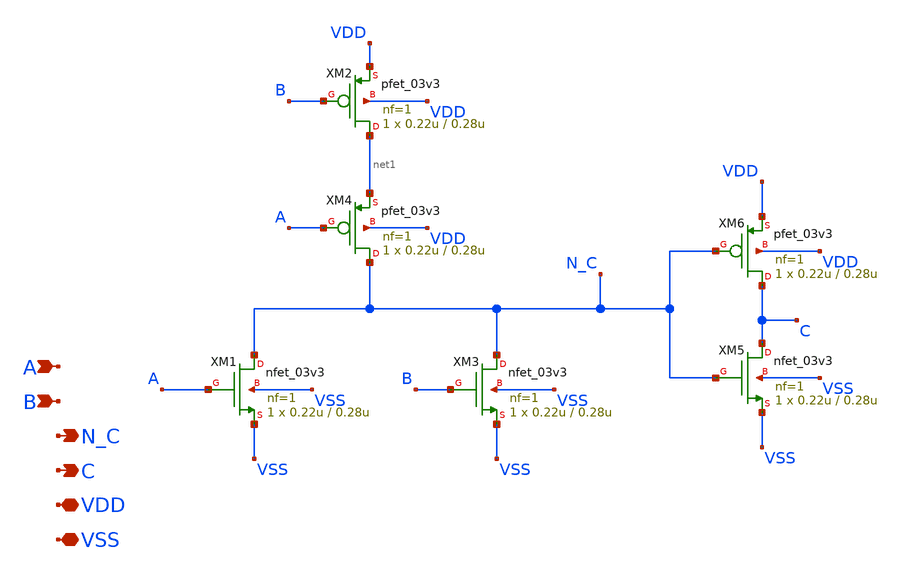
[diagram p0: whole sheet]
** sch_path: schematics/logic-gates/or/or.sch
**.subckt or A B N_C C VDD VSS
*.ipin A
*.ipin B
*.opin N_C
*.opin C
*.iopin VDD
*.iopin VSS
XM1 N_C A VSS VSS nfet_03v3 L=0.28u W=0.22u nf=1 ad='int((nf+1)/2) * W/nf * 0.18u' as='int((nf+2)/2) * W/nf * 0.18u'
+ pd='2*int((nf+1)/2) * (W/nf + 0.18u)' ps='2*int((nf+2)/2) * (W/nf + 0.18u)' nrd='0.18u / W' nrs='0.18u / W'
+ sa=0 sb=0 sd=0 m=1
XM2 net1 B VDD VDD pfet_03v3 L=0.28u W=0.22u nf=1 ad='int((nf+1)/2) * W/nf * 0.18u' as='int((nf+2)/2) * W/nf * 0.18u'
+ pd='2*int((nf+1)/2) * (W/nf + 0.18u)' ps='2*int((nf+2)/2) * (W/nf + 0.18u)' nrd='0.18u / W' nrs='0.18u / W'
+ sa=0 sb=0 sd=0 m=1
XM3 N_C B VSS VSS nfet_03v3 L=0.28u W=0.22u nf=1 ad='int((nf+1)/2) * W/nf * 0.18u' as='int((nf+2)/2) * W/nf * 0.18u'
+ pd='2*int((nf+1)/2) * (W/nf + 0.18u)' ps='2*int((nf+2)/2) * (W/nf + 0.18u)' nrd='0.18u / W' nrs='0.18u / W'
+ sa=0 sb=0 sd=0 m=1
XM4 N_C A net1 VDD pfet_03v3 L=0.28u W=0.22u nf=1 ad='int((nf+1)/2) * W/nf * 0.18u' as='int((nf+2)/2) * W/nf * 0.18u'
+ pd='2*int((nf+1)/2) * (W/nf + 0.18u)' ps='2*int((nf+2)/2) * (W/nf + 0.18u)' nrd='0.18u / W' nrs='0.18u / W'
+ sa=0 sb=0 sd=0 m=1
XM5 C N_C VSS VSS nfet_03v3 L=0.28u W=0.22u nf=1 ad='int((nf+1)/2) * W/nf * 0.18u' as='int((nf+2)/2) * W/nf * 0.18u'
+ pd='2*int((nf+1)/2) * (W/nf + 0.18u)' ps='2*int((nf+2)/2) * (W/nf + 0.18u)' nrd='0.18u / W' nrs='0.18u / W'
+ sa=0 sb=0 sd=0 m=1
XM6 C N_C VDD VDD pfet_03v3 L=0.28u W=0.22u nf=1 ad='int((nf+1)/2) * W/nf * 0.18u' as='int((nf+2)/2) * W/nf * 0.18u'
+ pd='2*int((nf+1)/2) * (W/nf + 0.18u)' ps='2*int((nf+2)/2) * (W/nf + 0.18u)' nrd='0.18u / W' nrs='0.18u / W'
+ sa=0 sb=0 sd=0 m=1
**.ends
.end
